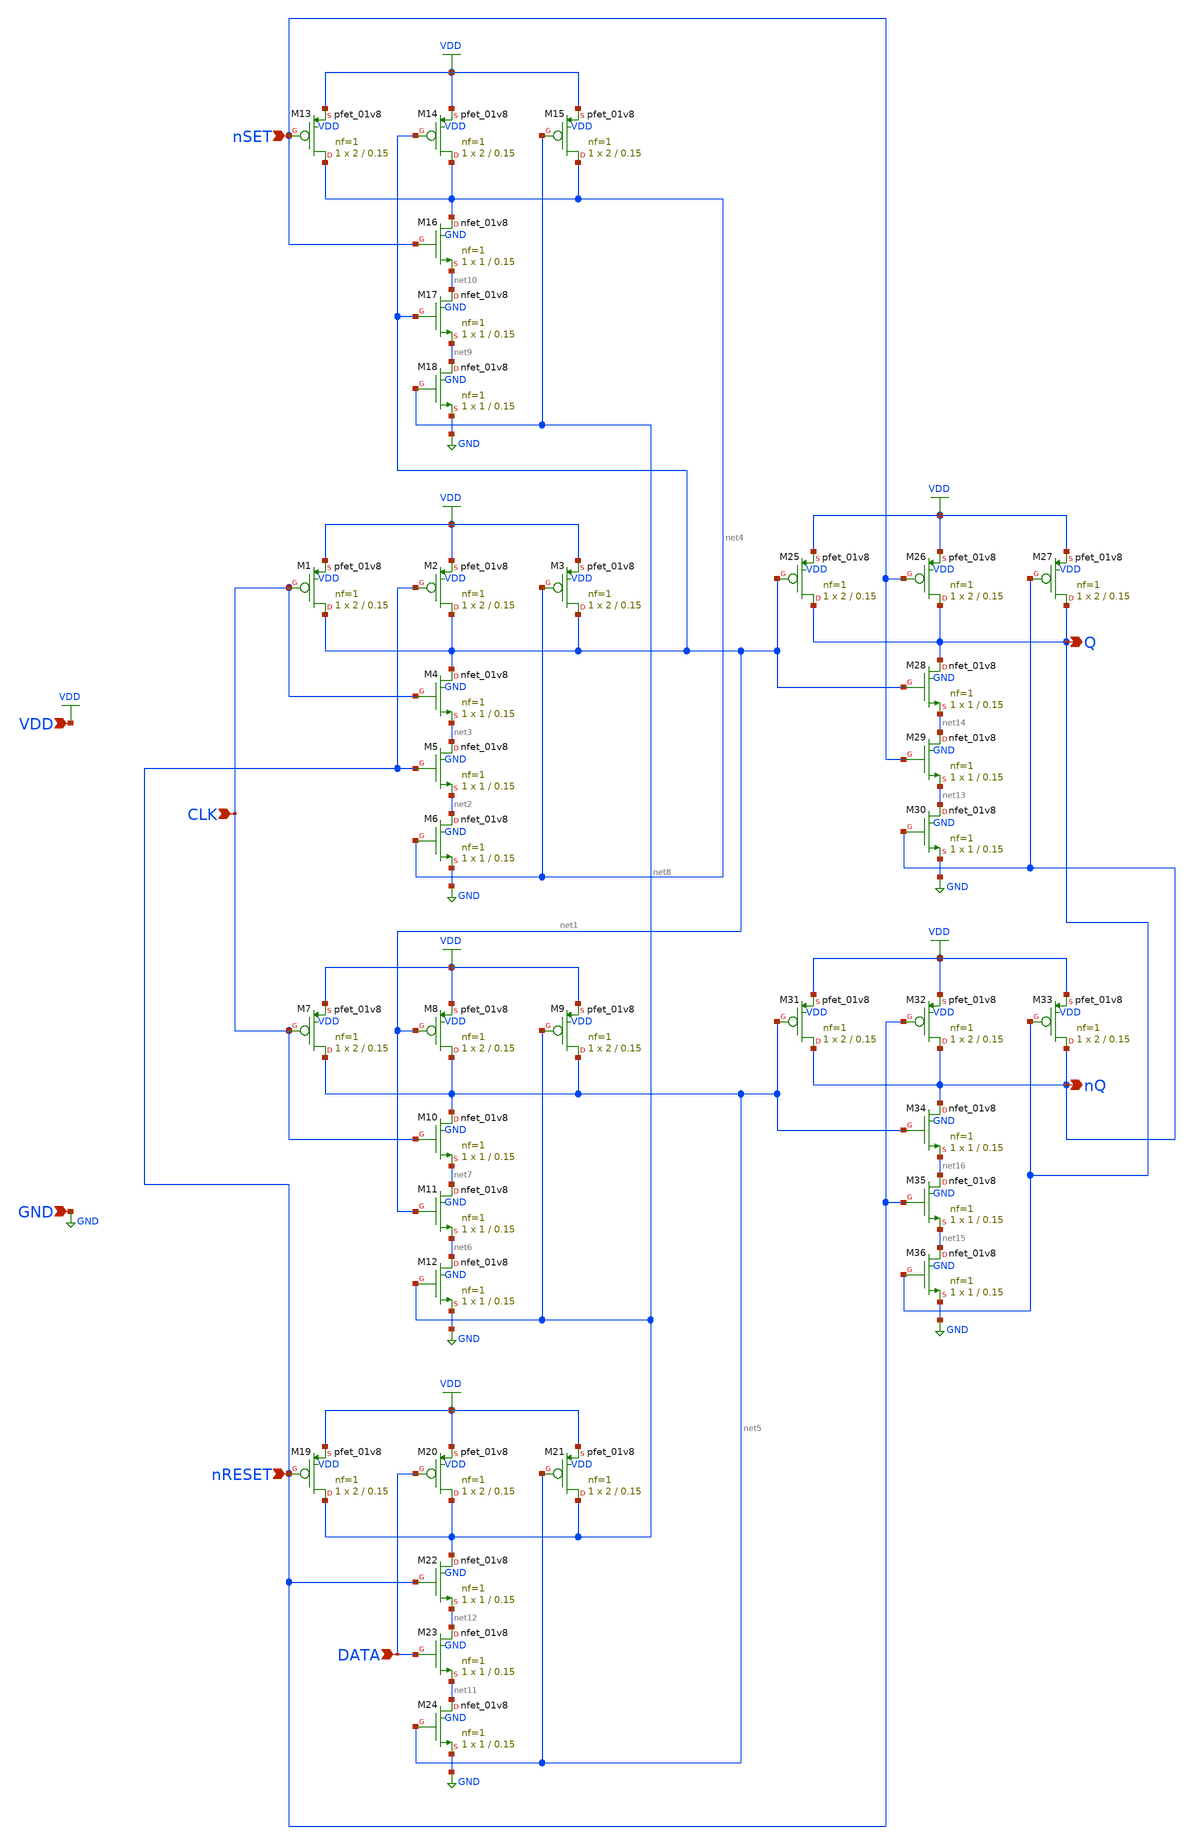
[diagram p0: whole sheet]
** sch_path: analog/schematics/DFF-async-nSet-nReset.sch
**.subckt DFF-async-nSet-nReset GND VDD CLK nSET nRESET Q nQ DATA
*.ipin GND
*.ipin VDD
*.ipin CLK
*.ipin nSET
*.ipin nRESET
*.opin Q
*.opin nQ
*.ipin DATA
XM1 net1 CLK VDD VDD sky130_fd_pr__pfet_01v8 L=0.15 W=2 nf=1 ad='int((1 + 1)/2) * 2 / 1 * 0.29' as='int((1 + 2)/2) * 2 / 1 * 0.29'
+ pd='2*int((1 + 1)/2) * (2 / 1 + 0.29)' ps='2*int((1 + 2)/2) * (2 / 1 + 0.29)' nrd='0.29 / 2 ' nrs='0.29 / 2 '
+ sa=0 sb=0 sd=0 mult=1 m=1
XM2 net1 nRESET VDD VDD sky130_fd_pr__pfet_01v8 L=0.15 W=2 nf=1 ad='int((1 + 1)/2) * 2 / 1 * 0.29' as='int((1 + 2)/2) * 2 / 1 * 0.29'
+ pd='2*int((1 + 1)/2) * (2 / 1 + 0.29)' ps='2*int((1 + 2)/2) * (2 / 1 + 0.29)' nrd='0.29 / 2 ' nrs='0.29 / 2 '
+ sa=0 sb=0 sd=0 mult=1 m=1
XM3 net1 net4 VDD VDD sky130_fd_pr__pfet_01v8 L=0.15 W=2 nf=1 ad='int((1 + 1)/2) * 2 / 1 * 0.29' as='int((1 + 2)/2) * 2 / 1 * 0.29'
+ pd='2*int((1 + 1)/2) * (2 / 1 + 0.29)' ps='2*int((1 + 2)/2) * (2 / 1 + 0.29)' nrd='0.29 / 2 ' nrs='0.29 / 2 '
+ sa=0 sb=0 sd=0 mult=1 m=1
XM4 net1 CLK net3 GND sky130_fd_pr__nfet_01v8 L=0.15 W=1 nf=1 ad='int((nf+1)/2) * W/nf * 0.29' as='int((nf+2)/2) * W/nf * 0.29'
+ pd='2*int((nf+1)/2) * (W/nf + 0.29)' ps='2*int((nf+2)/2) * (W/nf + 0.29)' nrd='0.29 / W' nrs='0.29 / W'
+ sa=0 sb=0 sd=0 mult=1 m=1
XM5 net3 nRESET net2 GND sky130_fd_pr__nfet_01v8 L=0.15 W=1 nf=1 ad='int((nf+1)/2) * W/nf * 0.29' as='int((nf+2)/2) * W/nf * 0.29'
+ pd='2*int((nf+1)/2) * (W/nf + 0.29)' ps='2*int((nf+2)/2) * (W/nf + 0.29)' nrd='0.29 / W' nrs='0.29 / W'
+ sa=0 sb=0 sd=0 mult=1 m=1
XM6 net2 net4 GND GND sky130_fd_pr__nfet_01v8 L=0.15 W=1 nf=1 ad='int((nf+1)/2) * W/nf * 0.29' as='int((nf+2)/2) * W/nf * 0.29'
+ pd='2*int((nf+1)/2) * (W/nf + 0.29)' ps='2*int((nf+2)/2) * (W/nf + 0.29)' nrd='0.29 / W' nrs='0.29 / W'
+ sa=0 sb=0 sd=0 mult=1 m=1
XM7 net5 CLK VDD VDD sky130_fd_pr__pfet_01v8 L=0.15 W=2 nf=1 ad='int((1 + 1)/2) * 2 / 1 * 0.29' as='int((1 + 2)/2) * 2 / 1 * 0.29'
+ pd='2*int((1 + 1)/2) * (2 / 1 + 0.29)' ps='2*int((1 + 2)/2) * (2 / 1 + 0.29)' nrd='0.29 / 2 ' nrs='0.29 / 2 '
+ sa=0 sb=0 sd=0 mult=1 m=1
XM8 net5 net1 VDD VDD sky130_fd_pr__pfet_01v8 L=0.15 W=2 nf=1 ad='int((1 + 1)/2) * 2 / 1 * 0.29' as='int((1 + 2)/2) * 2 / 1 * 0.29'
+ pd='2*int((1 + 1)/2) * (2 / 1 + 0.29)' ps='2*int((1 + 2)/2) * (2 / 1 + 0.29)' nrd='0.29 / 2 ' nrs='0.29 / 2 '
+ sa=0 sb=0 sd=0 mult=1 m=1
XM9 net5 net8 VDD VDD sky130_fd_pr__pfet_01v8 L=0.15 W=2 nf=1 ad='int((1 + 1)/2) * 2 / 1 * 0.29' as='int((1 + 2)/2) * 2 / 1 * 0.29'
+ pd='2*int((1 + 1)/2) * (2 / 1 + 0.29)' ps='2*int((1 + 2)/2) * (2 / 1 + 0.29)' nrd='0.29 / 2 ' nrs='0.29 / 2 '
+ sa=0 sb=0 sd=0 mult=1 m=1
XM10 net5 CLK net7 GND sky130_fd_pr__nfet_01v8 L=0.15 W=1 nf=1 ad='int((nf+1)/2) * W/nf * 0.29' as='int((nf+2)/2) * W/nf * 0.29'
+ pd='2*int((nf+1)/2) * (W/nf + 0.29)' ps='2*int((nf+2)/2) * (W/nf + 0.29)' nrd='0.29 / W' nrs='0.29 / W'
+ sa=0 sb=0 sd=0 mult=1 m=1
XM11 net7 net1 net6 GND sky130_fd_pr__nfet_01v8 L=0.15 W=1 nf=1 ad='int((nf+1)/2) * W/nf * 0.29' as='int((nf+2)/2) * W/nf * 0.29'
+ pd='2*int((nf+1)/2) * (W/nf + 0.29)' ps='2*int((nf+2)/2) * (W/nf + 0.29)' nrd='0.29 / W' nrs='0.29 / W'
+ sa=0 sb=0 sd=0 mult=1 m=1
XM12 net6 net8 GND GND sky130_fd_pr__nfet_01v8 L=0.15 W=1 nf=1 ad='int((nf+1)/2) * W/nf * 0.29' as='int((nf+2)/2) * W/nf * 0.29'
+ pd='2*int((nf+1)/2) * (W/nf + 0.29)' ps='2*int((nf+2)/2) * (W/nf + 0.29)' nrd='0.29 / W' nrs='0.29 / W'
+ sa=0 sb=0 sd=0 mult=1 m=1
XM13 net4 nSET VDD VDD sky130_fd_pr__pfet_01v8 L=0.15 W=2 nf=1 ad='int((1 + 1)/2) * 2 / 1 * 0.29' as='int((1 + 2)/2) * 2 / 1 * 0.29'
+ pd='2*int((1 + 1)/2) * (2 / 1 + 0.29)' ps='2*int((1 + 2)/2) * (2 / 1 + 0.29)' nrd='0.29 / 2 ' nrs='0.29 / 2 '
+ sa=0 sb=0 sd=0 mult=1 m=1
XM14 net4 net1 VDD VDD sky130_fd_pr__pfet_01v8 L=0.15 W=2 nf=1 ad='int((1 + 1)/2) * 2 / 1 * 0.29' as='int((1 + 2)/2) * 2 / 1 * 0.29'
+ pd='2*int((1 + 1)/2) * (2 / 1 + 0.29)' ps='2*int((1 + 2)/2) * (2 / 1 + 0.29)' nrd='0.29 / 2 ' nrs='0.29 / 2 '
+ sa=0 sb=0 sd=0 mult=1 m=1
XM15 net4 net8 VDD VDD sky130_fd_pr__pfet_01v8 L=0.15 W=2 nf=1 ad='int((1 + 1)/2) * 2 / 1 * 0.29' as='int((1 + 2)/2) * 2 / 1 * 0.29'
+ pd='2*int((1 + 1)/2) * (2 / 1 + 0.29)' ps='2*int((1 + 2)/2) * (2 / 1 + 0.29)' nrd='0.29 / 2 ' nrs='0.29 / 2 '
+ sa=0 sb=0 sd=0 mult=1 m=1
XM16 net4 nSET net10 GND sky130_fd_pr__nfet_01v8 L=0.15 W=1 nf=1 ad='int((nf+1)/2) * W/nf * 0.29' as='int((nf+2)/2) * W/nf * 0.29'
+ pd='2*int((nf+1)/2) * (W/nf + 0.29)' ps='2*int((nf+2)/2) * (W/nf + 0.29)' nrd='0.29 / W' nrs='0.29 / W'
+ sa=0 sb=0 sd=0 mult=1 m=1
XM17 net10 net1 net9 GND sky130_fd_pr__nfet_01v8 L=0.15 W=1 nf=1 ad='int((nf+1)/2) * W/nf * 0.29' as='int((nf+2)/2) * W/nf * 0.29'
+ pd='2*int((nf+1)/2) * (W/nf + 0.29)' ps='2*int((nf+2)/2) * (W/nf + 0.29)' nrd='0.29 / W' nrs='0.29 / W'
+ sa=0 sb=0 sd=0 mult=1 m=1
XM18 net9 net8 GND GND sky130_fd_pr__nfet_01v8 L=0.15 W=1 nf=1 ad='int((nf+1)/2) * W/nf * 0.29' as='int((nf+2)/2) * W/nf * 0.29'
+ pd='2*int((nf+1)/2) * (W/nf + 0.29)' ps='2*int((nf+2)/2) * (W/nf + 0.29)' nrd='0.29 / W' nrs='0.29 / W'
+ sa=0 sb=0 sd=0 mult=1 m=1
XM19 net8 nRESET VDD VDD sky130_fd_pr__pfet_01v8 L=0.15 W=2 nf=1 ad='int((1 + 1)/2) * 2 / 1 * 0.29' as='int((1 + 2)/2) * 2 / 1 * 0.29'
+ pd='2*int((1 + 1)/2) * (2 / 1 + 0.29)' ps='2*int((1 + 2)/2) * (2 / 1 + 0.29)' nrd='0.29 / 2 ' nrs='0.29 / 2 '
+ sa=0 sb=0 sd=0 mult=1 m=1
XM20 net8 DATA VDD VDD sky130_fd_pr__pfet_01v8 L=0.15 W=2 nf=1 ad='int((1 + 1)/2) * 2 / 1 * 0.29' as='int((1 + 2)/2) * 2 / 1 * 0.29'
+ pd='2*int((1 + 1)/2) * (2 / 1 + 0.29)' ps='2*int((1 + 2)/2) * (2 / 1 + 0.29)' nrd='0.29 / 2 ' nrs='0.29 / 2 '
+ sa=0 sb=0 sd=0 mult=1 m=1
XM21 net8 net5 VDD VDD sky130_fd_pr__pfet_01v8 L=0.15 W=2 nf=1 ad='int((1 + 1)/2) * 2 / 1 * 0.29' as='int((1 + 2)/2) * 2 / 1 * 0.29'
+ pd='2*int((1 + 1)/2) * (2 / 1 + 0.29)' ps='2*int((1 + 2)/2) * (2 / 1 + 0.29)' nrd='0.29 / 2 ' nrs='0.29 / 2 '
+ sa=0 sb=0 sd=0 mult=1 m=1
XM22 net8 nRESET net12 GND sky130_fd_pr__nfet_01v8 L=0.15 W=1 nf=1 ad='int((nf+1)/2) * W/nf * 0.29' as='int((nf+2)/2) * W/nf * 0.29'
+ pd='2*int((nf+1)/2) * (W/nf + 0.29)' ps='2*int((nf+2)/2) * (W/nf + 0.29)' nrd='0.29 / W' nrs='0.29 / W'
+ sa=0 sb=0 sd=0 mult=1 m=1
XM23 net12 DATA net11 GND sky130_fd_pr__nfet_01v8 L=0.15 W=1 nf=1 ad='int((nf+1)/2) * W/nf * 0.29' as='int((nf+2)/2) * W/nf * 0.29'
+ pd='2*int((nf+1)/2) * (W/nf + 0.29)' ps='2*int((nf+2)/2) * (W/nf + 0.29)' nrd='0.29 / W' nrs='0.29 / W'
+ sa=0 sb=0 sd=0 mult=1 m=1
XM24 net11 net5 GND GND sky130_fd_pr__nfet_01v8 L=0.15 W=1 nf=1 ad='int((nf+1)/2) * W/nf * 0.29' as='int((nf+2)/2) * W/nf * 0.29'
+ pd='2*int((nf+1)/2) * (W/nf + 0.29)' ps='2*int((nf+2)/2) * (W/nf + 0.29)' nrd='0.29 / W' nrs='0.29 / W'
+ sa=0 sb=0 sd=0 mult=1 m=1
XM25 Q net1 VDD VDD sky130_fd_pr__pfet_01v8 L=0.15 W=2 nf=1 ad='int((1 + 1)/2) * 2 / 1 * 0.29' as='int((1 + 2)/2) * 2 / 1 * 0.29'
+ pd='2*int((1 + 1)/2) * (2 / 1 + 0.29)' ps='2*int((1 + 2)/2) * (2 / 1 + 0.29)' nrd='0.29 / 2 ' nrs='0.29 / 2 '
+ sa=0 sb=0 sd=0 mult=1 m=1
XM26 Q nSET VDD VDD sky130_fd_pr__pfet_01v8 L=0.15 W=2 nf=1 ad='int((1 + 1)/2) * 2 / 1 * 0.29' as='int((1 + 2)/2) * 2 / 1 * 0.29'
+ pd='2*int((1 + 1)/2) * (2 / 1 + 0.29)' ps='2*int((1 + 2)/2) * (2 / 1 + 0.29)' nrd='0.29 / 2 ' nrs='0.29 / 2 '
+ sa=0 sb=0 sd=0 mult=1 m=1
XM27 Q nQ VDD VDD sky130_fd_pr__pfet_01v8 L=0.15 W=2 nf=1 ad='int((1 + 1)/2) * 2 / 1 * 0.29' as='int((1 + 2)/2) * 2 / 1 * 0.29'
+ pd='2*int((1 + 1)/2) * (2 / 1 + 0.29)' ps='2*int((1 + 2)/2) * (2 / 1 + 0.29)' nrd='0.29 / 2 ' nrs='0.29 / 2 '
+ sa=0 sb=0 sd=0 mult=1 m=1
XM28 Q net1 net14 GND sky130_fd_pr__nfet_01v8 L=0.15 W=1 nf=1 ad='int((nf+1)/2) * W/nf * 0.29' as='int((nf+2)/2) * W/nf * 0.29'
+ pd='2*int((nf+1)/2) * (W/nf + 0.29)' ps='2*int((nf+2)/2) * (W/nf + 0.29)' nrd='0.29 / W' nrs='0.29 / W'
+ sa=0 sb=0 sd=0 mult=1 m=1
XM29 net14 nSET net13 GND sky130_fd_pr__nfet_01v8 L=0.15 W=1 nf=1 ad='int((nf+1)/2) * W/nf * 0.29' as='int((nf+2)/2) * W/nf * 0.29'
+ pd='2*int((nf+1)/2) * (W/nf + 0.29)' ps='2*int((nf+2)/2) * (W/nf + 0.29)' nrd='0.29 / W' nrs='0.29 / W'
+ sa=0 sb=0 sd=0 mult=1 m=1
XM30 net13 nQ GND GND sky130_fd_pr__nfet_01v8 L=0.15 W=1 nf=1 ad='int((nf+1)/2) * W/nf * 0.29' as='int((nf+2)/2) * W/nf * 0.29'
+ pd='2*int((nf+1)/2) * (W/nf + 0.29)' ps='2*int((nf+2)/2) * (W/nf + 0.29)' nrd='0.29 / W' nrs='0.29 / W'
+ sa=0 sb=0 sd=0 mult=1 m=1
XM31 nQ net5 VDD VDD sky130_fd_pr__pfet_01v8 L=0.15 W=2 nf=1 ad='int((1 + 1)/2) * 2 / 1 * 0.29' as='int((1 + 2)/2) * 2 / 1 * 0.29'
+ pd='2*int((1 + 1)/2) * (2 / 1 + 0.29)' ps='2*int((1 + 2)/2) * (2 / 1 + 0.29)' nrd='0.29 / 2 ' nrs='0.29 / 2 '
+ sa=0 sb=0 sd=0 mult=1 m=1
XM32 nQ nRESET VDD VDD sky130_fd_pr__pfet_01v8 L=0.15 W=2 nf=1 ad='int((1 + 1)/2) * 2 / 1 * 0.29' as='int((1 + 2)/2) * 2 / 1 * 0.29'
+ pd='2*int((1 + 1)/2) * (2 / 1 + 0.29)' ps='2*int((1 + 2)/2) * (2 / 1 + 0.29)' nrd='0.29 / 2 ' nrs='0.29 / 2 '
+ sa=0 sb=0 sd=0 mult=1 m=1
XM33 nQ Q VDD VDD sky130_fd_pr__pfet_01v8 L=0.15 W=2 nf=1 ad='int((1 + 1)/2) * 2 / 1 * 0.29' as='int((1 + 2)/2) * 2 / 1 * 0.29'
+ pd='2*int((1 + 1)/2) * (2 / 1 + 0.29)' ps='2*int((1 + 2)/2) * (2 / 1 + 0.29)' nrd='0.29 / 2 ' nrs='0.29 / 2 '
+ sa=0 sb=0 sd=0 mult=1 m=1
XM34 nQ net5 net16 GND sky130_fd_pr__nfet_01v8 L=0.15 W=1 nf=1 ad='int((nf+1)/2) * W/nf * 0.29' as='int((nf+2)/2) * W/nf * 0.29'
+ pd='2*int((nf+1)/2) * (W/nf + 0.29)' ps='2*int((nf+2)/2) * (W/nf + 0.29)' nrd='0.29 / W' nrs='0.29 / W'
+ sa=0 sb=0 sd=0 mult=1 m=1
XM35 net16 nRESET net15 GND sky130_fd_pr__nfet_01v8 L=0.15 W=1 nf=1 ad='int((nf+1)/2) * W/nf * 0.29'
+ as='int((nf+2)/2) * W/nf * 0.29' pd='2*int((nf+1)/2) * (W/nf + 0.29)' ps='2*int((nf+2)/2) * (W/nf + 0.29)'
+ nrd='0.29 / W' nrs='0.29 / W' sa=0 sb=0 sd=0 mult=1 m=1
XM36 net15 Q GND GND sky130_fd_pr__nfet_01v8 L=0.15 W=1 nf=1 ad='int((nf+1)/2) * W/nf * 0.29' as='int((nf+2)/2) * W/nf * 0.29'
+ pd='2*int((nf+1)/2) * (W/nf + 0.29)' ps='2*int((nf+2)/2) * (W/nf + 0.29)' nrd='0.29 / W' nrs='0.29 / W'
+ sa=0 sb=0 sd=0 mult=1 m=1
**.ends
.GLOBAL GND
.GLOBAL VDD
.end
